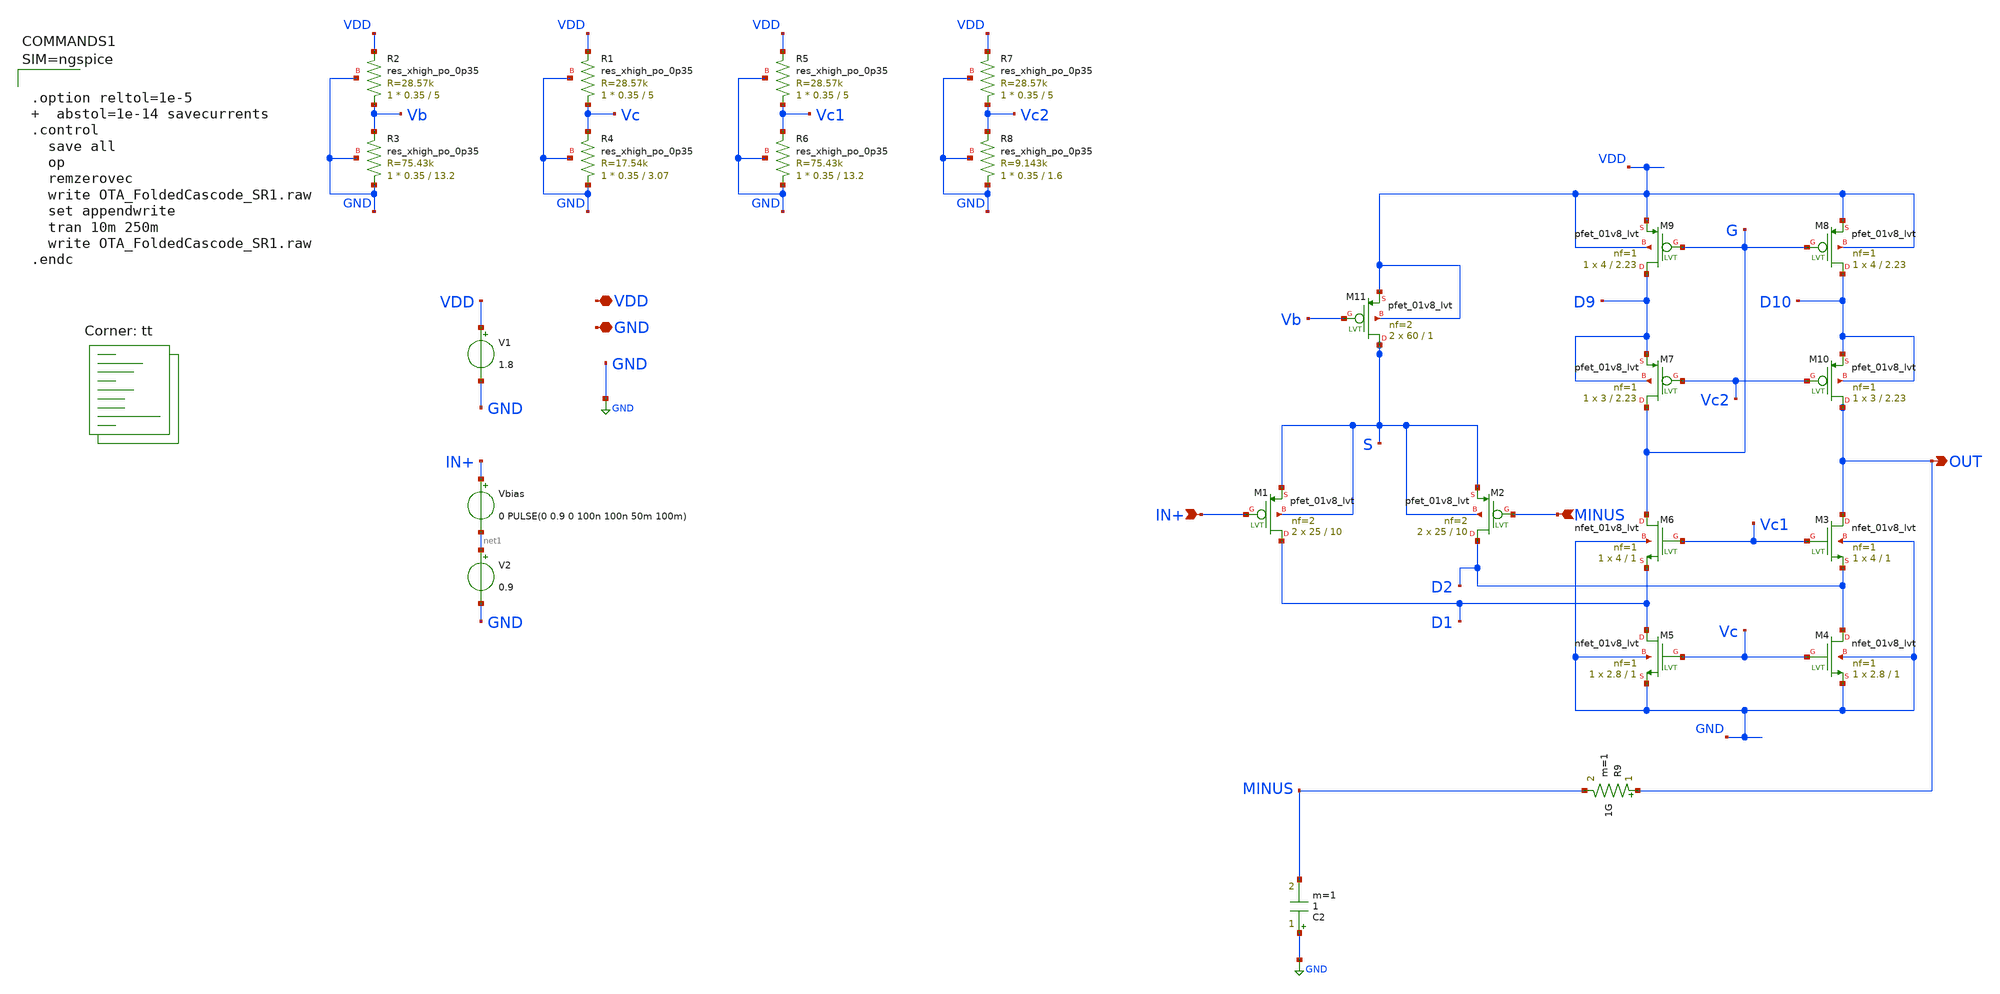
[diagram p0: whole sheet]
** sch_path: xschem/OTA_FoldedCascode_SR1.sch
**.subckt OTA_FoldedCascode_SR1 VDD GND IN+ MINUS OUT
*.iopin VDD
*.iopin GND
*.ipin IN+
*.ipin MINUS
*.opin OUT
V1 VDD GND 1.8
Vbias IN+ net1 0 PULSE(0 0.9 0 100n 100n 50m 100m)
V2 net1 GND 0.9
XM11 S Vb VDD VDD sky130_fd_pr__pfet_01v8_lvt L=1 W=60 nf=2 ad='int((nf+1)/2) * W/nf * 0.29' as='int((nf+2)/2) * W/nf * 0.29'
+ pd='2*int((nf+1)/2) * (W/nf + 0.29)' ps='2*int((nf+2)/2) * (W/nf + 0.29)' nrd='0.29 / W' nrs='0.29 / W'
+ sa=0 sb=0 sd=0 mult=2 m=2
XM1 D1 IN+ S S sky130_fd_pr__pfet_01v8_lvt L=10 W=25 nf=2 ad='int((nf+1)/2) * W/nf * 0.29' as='int((nf+2)/2) * W/nf * 0.29'
+ pd='2*int((nf+1)/2) * (W/nf + 0.29)' ps='2*int((nf+2)/2) * (W/nf + 0.29)' nrd='0.29 / W' nrs='0.29 / W'
+ sa=0 sb=0 sd=0 mult=2 m=2
XM2 D2 MINUS S S sky130_fd_pr__pfet_01v8_lvt L=10 W=25 nf=2 ad='int((nf+1)/2) * W/nf * 0.29' as='int((nf+2)/2) * W/nf * 0.29'
+ pd='2*int((nf+1)/2) * (W/nf + 0.29)' ps='2*int((nf+2)/2) * (W/nf + 0.29)' nrd='0.29 / W' nrs='0.29 / W'
+ sa=0 sb=0 sd=0 mult=2 m=2
XM3 OUT Vc1 D2 GND sky130_fd_pr__nfet_01v8_lvt L=1 W=4 nf=1 ad='int((nf+1)/2) * W/nf * 0.29' as='int((nf+2)/2) * W/nf * 0.29'
+ pd='2*int((nf+1)/2) * (W/nf + 0.29)' ps='2*int((nf+2)/2) * (W/nf + 0.29)' nrd='0.29 / W' nrs='0.29 / W'
+ sa=0 sb=0 sd=0 mult=1 m=1
XM4 D2 Vc GND GND sky130_fd_pr__nfet_01v8_lvt L=1 W=2.8 nf=1 ad='int((nf+1)/2) * W/nf * 0.29' as='int((nf+2)/2) * W/nf * 0.29'
+ pd='2*int((nf+1)/2) * (W/nf + 0.29)' ps='2*int((nf+2)/2) * (W/nf + 0.29)' nrd='0.29 / W' nrs='0.29 / W'
+ sa=0 sb=0 sd=0 mult=1 m=1
XM5 D1 Vc GND GND sky130_fd_pr__nfet_01v8_lvt L=1 W=2.8 nf=1 ad='int((nf+1)/2) * W/nf * 0.29' as='int((nf+2)/2) * W/nf * 0.29'
+ pd='2*int((nf+1)/2) * (W/nf + 0.29)' ps='2*int((nf+2)/2) * (W/nf + 0.29)' nrd='0.29 / W' nrs='0.29 / W'
+ sa=0 sb=0 sd=0 mult=1 m=1
XM6 G Vc1 D1 GND sky130_fd_pr__nfet_01v8_lvt L=1 W=4 nf=1 ad='int((nf+1)/2) * W/nf * 0.29' as='int((nf+2)/2) * W/nf * 0.29'
+ pd='2*int((nf+1)/2) * (W/nf + 0.29)' ps='2*int((nf+2)/2) * (W/nf + 0.29)' nrd='0.29 / W' nrs='0.29 / W'
+ sa=0 sb=0 sd=0 mult=1 m=1
XM7 G Vc2 D9 D9 sky130_fd_pr__pfet_01v8_lvt L=2.23 W=3 nf=1 ad='int((nf+1)/2) * W/nf * 0.29' as='int((nf+2)/2) * W/nf * 0.29'
+ pd='2*int((nf+1)/2) * (W/nf + 0.29)' ps='2*int((nf+2)/2) * (W/nf + 0.29)' nrd='0.29 / W' nrs='0.29 / W'
+ sa=0 sb=0 sd=0 mult=1 m=1
XM9 D9 G VDD VDD sky130_fd_pr__pfet_01v8_lvt L=2.23 W=4 nf=1 ad='int((nf+1)/2) * W/nf * 0.29' as='int((nf+2)/2) * W/nf * 0.29'
+ pd='2*int((nf+1)/2) * (W/nf + 0.29)' ps='2*int((nf+2)/2) * (W/nf + 0.29)' nrd='0.29 / W' nrs='0.29 / W'
+ sa=0 sb=0 sd=0 mult=1 m=1
XM8 D10 G VDD VDD sky130_fd_pr__pfet_01v8_lvt L=2.23 W=4 nf=1 ad='int((nf+1)/2) * W/nf * 0.29' as='int((nf+2)/2) * W/nf * 0.29'
+ pd='2*int((nf+1)/2) * (W/nf + 0.29)' ps='2*int((nf+2)/2) * (W/nf + 0.29)' nrd='0.29 / W' nrs='0.29 / W'
+ sa=0 sb=0 sd=0 mult=1 m=1
XM10 OUT Vc2 D10 D10 sky130_fd_pr__pfet_01v8_lvt L=2.23 W=3 nf=1 ad='int((nf+1)/2) * W/nf * 0.29' as='int((nf+2)/2) * W/nf * 0.29'
+ pd='2*int((nf+1)/2) * (W/nf + 0.29)' ps='2*int((nf+2)/2) * (W/nf + 0.29)' nrd='0.29 / W' nrs='0.29 / W'
+ sa=0 sb=0 sd=0 mult=1 m=1
XR2 Vb VDD GND sky130_fd_pr__res_xhigh_po_0p35 L=5 mult=1 m=1
XR3 GND Vb GND sky130_fd_pr__res_xhigh_po_0p35 L=13.2 mult=1 m=1
XR1 Vc VDD GND sky130_fd_pr__res_xhigh_po_0p35 L=5 mult=1 m=1
XR4 GND Vc GND sky130_fd_pr__res_xhigh_po_0p35 L=3.07 mult=1 m=1
XR5 Vc1 VDD GND sky130_fd_pr__res_xhigh_po_0p35 L=5 mult=1 m=1
XR6 GND Vc1 GND sky130_fd_pr__res_xhigh_po_0p35 L=13.2 mult=1 m=1
XR7 Vc2 VDD GND sky130_fd_pr__res_xhigh_po_0p35 L=5 mult=1 m=1
XR8 GND Vc2 GND sky130_fd_pr__res_xhigh_po_0p35 L=1.6 mult=1 m=1
C2 GND MINUS 1 m=1
R9 OUT MINUS 1G m=1
**** begin user architecture code



.option reltol=1e-5   abstol=1e-14 savecurrents
.control
  save all
  op
  remzerovec
  write OTA_FoldedCascode_SR1.raw
  set appendwrite
  tran 10m 250m
  write OTA_FoldedCascode_SR1.raw
.endc



.lib $::SKYWATER_MODELS/sky130.lib.spice tt
**** end user architecture code
**.ends
.GLOBAL GND
.end
